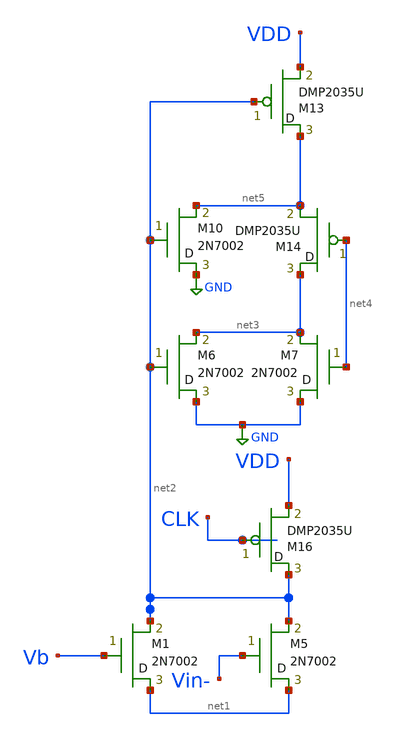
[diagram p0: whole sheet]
** sch_path: ISSCC25/submitted_notebooks/MicroNina/sch/half_Miyahara.sch
**.subckt half_Miyahara
M5 net1 Vin- net2 M2N7002 m=1
M1 net1 Vb net2 M2N7002 m=1
M6 GND net2 net3 M2N7002 m=1
M7 GND net4 net3 M2N7002 m=1
M10 GND net2 net5 M2N7002 m=1
M13 net5 net2 VDD DMP2035U m=1
M14 net3 net4 net5 DMP2035U m=1
M16 net2 CLK VDD DMP2035U m=1
**.ends
.GLOBAL GND
.end
